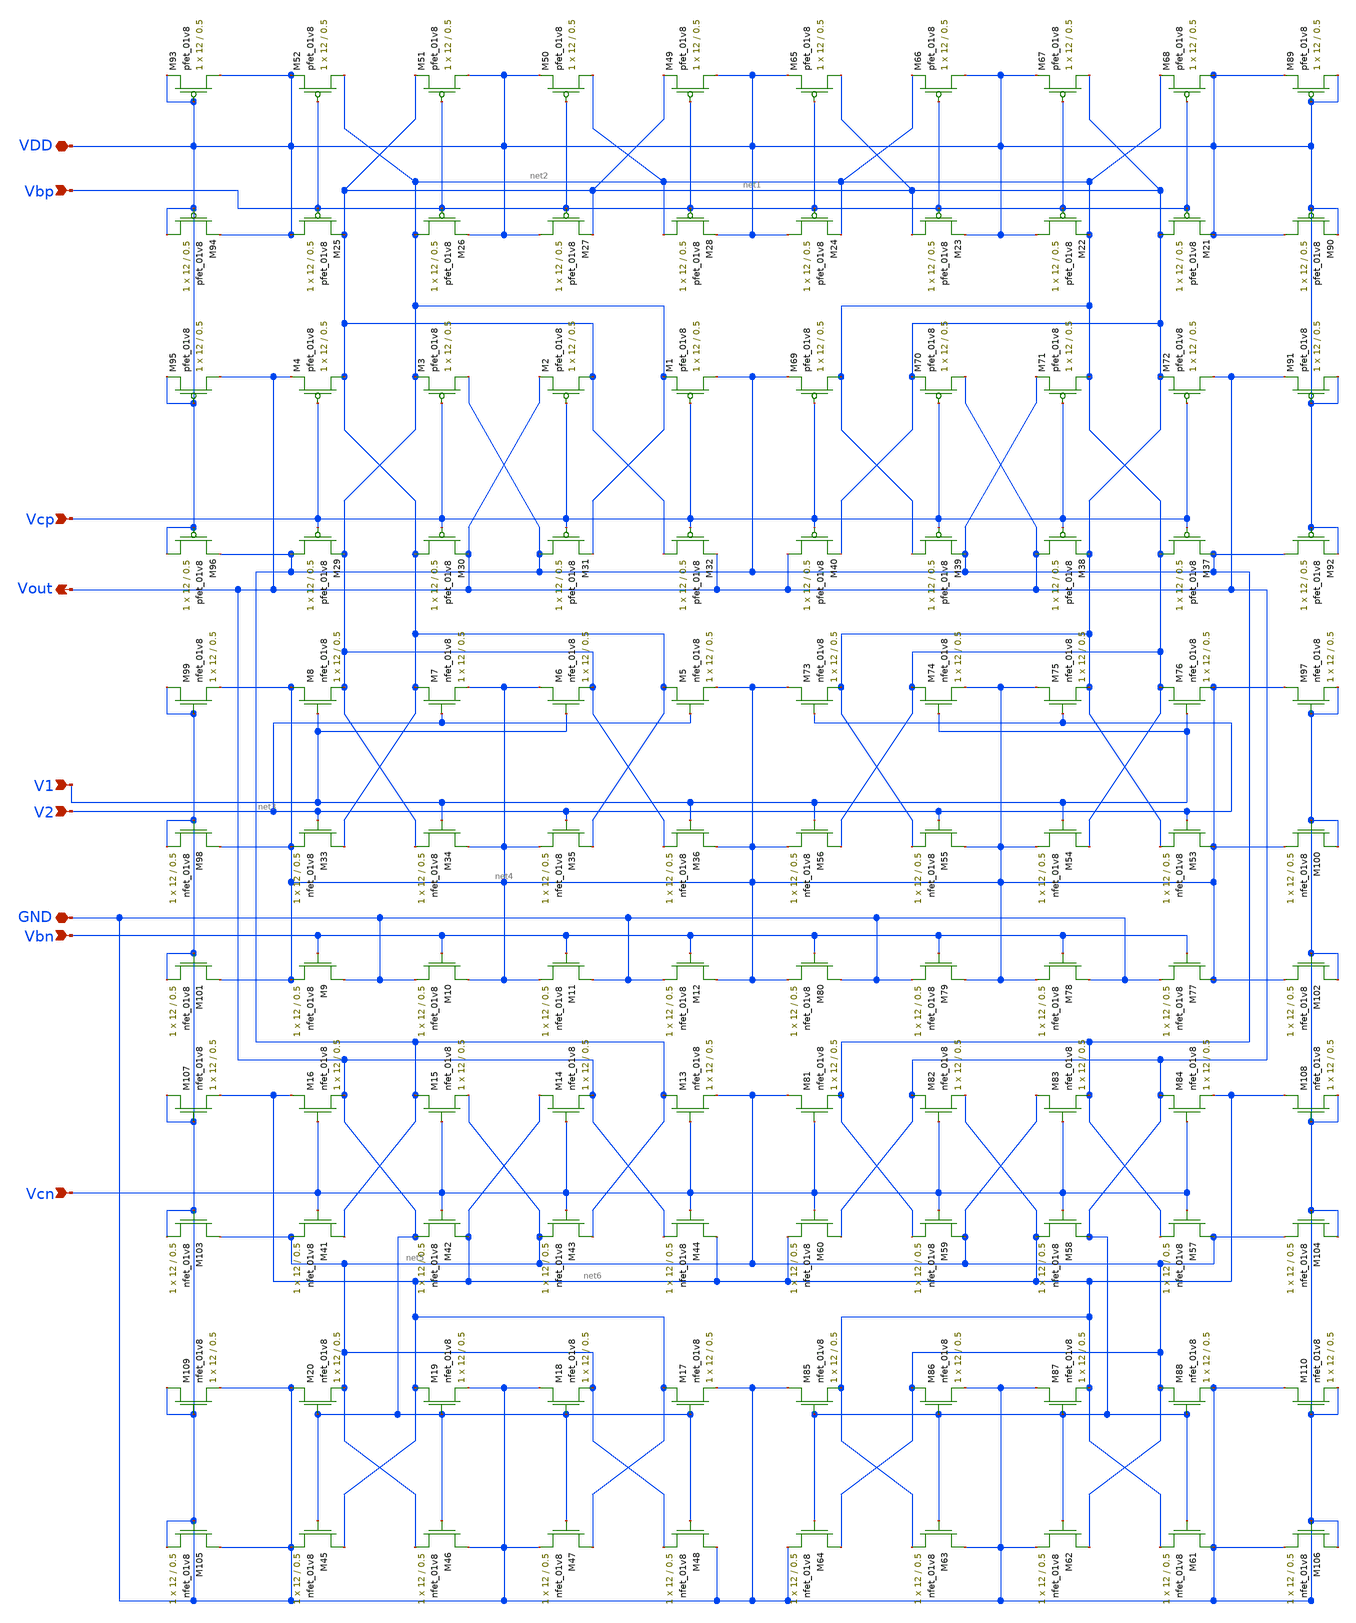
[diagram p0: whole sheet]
** sch_path: Miniproject3/layout&schematics/Folded_cascode_differential_amplifier.sch
**.subckt Folded_cascode_differential_amplifier Vbp Vcp Vout V1 V2 Vbn VDD GND Vcn
*.ipin Vbp
*.ipin Vcp
*.opin Vout
*.ipin V1
*.ipin V2
*.ipin Vbn
*.iopin VDD
*.iopin GND
*.ipin Vcn
XM52 net2 Vbp VDD VDD sky130_fd_pr__pfet_01v8 L=0.5 W=12 nf=1 ad='int((nf+1)/2) * W/nf * 0.29' as='int((nf+2)/2) * W/nf * 0.29'
+ pd='2*int((nf+1)/2) * (W/nf + 0.29)' ps='2*int((nf+2)/2) * (W/nf + 0.29)' nrd='0.29 / W' nrs='0.29 / W'
+ sa=0 sb=0 sd=0 mult=1 m=1
XM51 VDD Vbp net1 VDD sky130_fd_pr__pfet_01v8 L=0.5 W=12 nf=1 ad='int((nf+1)/2) * W/nf * 0.29' as='int((nf+2)/2) * W/nf * 0.29'
+ pd='2*int((nf+1)/2) * (W/nf + 0.29)' ps='2*int((nf+2)/2) * (W/nf + 0.29)' nrd='0.29 / W' nrs='0.29 / W'
+ sa=0 sb=0 sd=0 mult=1 m=1
XM50 net2 Vbp VDD VDD sky130_fd_pr__pfet_01v8 L=0.5 W=12 nf=1 ad='int((nf+1)/2) * W/nf * 0.29' as='int((nf+2)/2) * W/nf * 0.29'
+ pd='2*int((nf+1)/2) * (W/nf + 0.29)' ps='2*int((nf+2)/2) * (W/nf + 0.29)' nrd='0.29 / W' nrs='0.29 / W'
+ sa=0 sb=0 sd=0 mult=1 m=1
XM49 VDD Vbp net1 VDD sky130_fd_pr__pfet_01v8 L=0.5 W=12 nf=1 ad='int((nf+1)/2) * W/nf * 0.29' as='int((nf+2)/2) * W/nf * 0.29'
+ pd='2*int((nf+1)/2) * (W/nf + 0.29)' ps='2*int((nf+2)/2) * (W/nf + 0.29)' nrd='0.29 / W' nrs='0.29 / W'
+ sa=0 sb=0 sd=0 mult=1 m=1
XM65 net1 Vbp VDD VDD sky130_fd_pr__pfet_01v8 L=0.5 W=12 nf=1 ad='int((nf+1)/2) * W/nf * 0.29' as='int((nf+2)/2) * W/nf * 0.29'
+ pd='2*int((nf+1)/2) * (W/nf + 0.29)' ps='2*int((nf+2)/2) * (W/nf + 0.29)' nrd='0.29 / W' nrs='0.29 / W'
+ sa=0 sb=0 sd=0 mult=1 m=1
XM66 VDD Vbp net2 VDD sky130_fd_pr__pfet_01v8 L=0.5 W=12 nf=1 ad='int((nf+1)/2) * W/nf * 0.29' as='int((nf+2)/2) * W/nf * 0.29'
+ pd='2*int((nf+1)/2) * (W/nf + 0.29)' ps='2*int((nf+2)/2) * (W/nf + 0.29)' nrd='0.29 / W' nrs='0.29 / W'
+ sa=0 sb=0 sd=0 mult=1 m=1
XM67 net1 Vbp VDD VDD sky130_fd_pr__pfet_01v8 L=0.5 W=12 nf=1 ad='int((nf+1)/2) * W/nf * 0.29' as='int((nf+2)/2) * W/nf * 0.29'
+ pd='2*int((nf+1)/2) * (W/nf + 0.29)' ps='2*int((nf+2)/2) * (W/nf + 0.29)' nrd='0.29 / W' nrs='0.29 / W'
+ sa=0 sb=0 sd=0 mult=1 m=1
XM68 VDD Vbp net2 VDD sky130_fd_pr__pfet_01v8 L=0.5 W=12 nf=1 ad='int((nf+1)/2) * W/nf * 0.29' as='int((nf+2)/2) * W/nf * 0.29'
+ pd='2*int((nf+1)/2) * (W/nf + 0.29)' ps='2*int((nf+2)/2) * (W/nf + 0.29)' nrd='0.29 / W' nrs='0.29 / W'
+ sa=0 sb=0 sd=0 mult=1 m=1
XM89 VDD VDD VDD VDD sky130_fd_pr__pfet_01v8 L=0.5 W=12 nf=1 ad='int((nf+1)/2) * W/nf * 0.29' as='int((nf+2)/2) * W/nf * 0.29'
+ pd='2*int((nf+1)/2) * (W/nf + 0.29)' ps='2*int((nf+2)/2) * (W/nf + 0.29)' nrd='0.29 / W' nrs='0.29 / W'
+ sa=0 sb=0 sd=0 mult=1 m=1
XM93 VDD VDD VDD VDD sky130_fd_pr__pfet_01v8 L=0.5 W=12 nf=1 ad='int((nf+1)/2) * W/nf * 0.29' as='int((nf+2)/2) * W/nf * 0.29'
+ pd='2*int((nf+1)/2) * (W/nf + 0.29)' ps='2*int((nf+2)/2) * (W/nf + 0.29)' nrd='0.29 / W' nrs='0.29 / W'
+ sa=0 sb=0 sd=0 mult=1 m=1
XM94 VDD VDD VDD VDD sky130_fd_pr__pfet_01v8 L=0.5 W=12 nf=1 ad='int((nf+1)/2) * W/nf * 0.29' as='int((nf+2)/2) * W/nf * 0.29'
+ pd='2*int((nf+1)/2) * (W/nf + 0.29)' ps='2*int((nf+2)/2) * (W/nf + 0.29)' nrd='0.29 / W' nrs='0.29 / W'
+ sa=0 sb=0 sd=0 mult=1 m=1
XM25 VDD Vbp net1 VDD sky130_fd_pr__pfet_01v8 L=0.5 W=12 nf=1 ad='int((nf+1)/2) * W/nf * 0.29' as='int((nf+2)/2) * W/nf * 0.29'
+ pd='2*int((nf+1)/2) * (W/nf + 0.29)' ps='2*int((nf+2)/2) * (W/nf + 0.29)' nrd='0.29 / W' nrs='0.29 / W'
+ sa=0 sb=0 sd=0 mult=1 m=1
XM26 net2 Vbp VDD VDD sky130_fd_pr__pfet_01v8 L=0.5 W=12 nf=1 ad='int((nf+1)/2) * W/nf * 0.29' as='int((nf+2)/2) * W/nf * 0.29'
+ pd='2*int((nf+1)/2) * (W/nf + 0.29)' ps='2*int((nf+2)/2) * (W/nf + 0.29)' nrd='0.29 / W' nrs='0.29 / W'
+ sa=0 sb=0 sd=0 mult=1 m=1
XM27 VDD Vbp net1 VDD sky130_fd_pr__pfet_01v8 L=0.5 W=12 nf=1 ad='int((nf+1)/2) * W/nf * 0.29' as='int((nf+2)/2) * W/nf * 0.29'
+ pd='2*int((nf+1)/2) * (W/nf + 0.29)' ps='2*int((nf+2)/2) * (W/nf + 0.29)' nrd='0.29 / W' nrs='0.29 / W'
+ sa=0 sb=0 sd=0 mult=1 m=1
XM28 net2 Vbp VDD VDD sky130_fd_pr__pfet_01v8 L=0.5 W=12 nf=1 ad='int((nf+1)/2) * W/nf * 0.29' as='int((nf+2)/2) * W/nf * 0.29'
+ pd='2*int((nf+1)/2) * (W/nf + 0.29)' ps='2*int((nf+2)/2) * (W/nf + 0.29)' nrd='0.29 / W' nrs='0.29 / W'
+ sa=0 sb=0 sd=0 mult=1 m=1
XM24 VDD Vbp net2 VDD sky130_fd_pr__pfet_01v8 L=0.5 W=12 nf=1 ad='int((nf+1)/2) * W/nf * 0.29' as='int((nf+2)/2) * W/nf * 0.29'
+ pd='2*int((nf+1)/2) * (W/nf + 0.29)' ps='2*int((nf+2)/2) * (W/nf + 0.29)' nrd='0.29 / W' nrs='0.29 / W'
+ sa=0 sb=0 sd=0 mult=1 m=1
XM23 net1 Vbp VDD VDD sky130_fd_pr__pfet_01v8 L=0.5 W=12 nf=1 ad='int((nf+1)/2) * W/nf * 0.29' as='int((nf+2)/2) * W/nf * 0.29'
+ pd='2*int((nf+1)/2) * (W/nf + 0.29)' ps='2*int((nf+2)/2) * (W/nf + 0.29)' nrd='0.29 / W' nrs='0.29 / W'
+ sa=0 sb=0 sd=0 mult=1 m=1
XM22 VDD Vbp net2 VDD sky130_fd_pr__pfet_01v8 L=0.5 W=12 nf=1 ad='int((nf+1)/2) * W/nf * 0.29' as='int((nf+2)/2) * W/nf * 0.29'
+ pd='2*int((nf+1)/2) * (W/nf + 0.29)' ps='2*int((nf+2)/2) * (W/nf + 0.29)' nrd='0.29 / W' nrs='0.29 / W'
+ sa=0 sb=0 sd=0 mult=1 m=1
XM21 net1 Vbp VDD VDD sky130_fd_pr__pfet_01v8 L=0.5 W=12 nf=1 ad='int((nf+1)/2) * W/nf * 0.29' as='int((nf+2)/2) * W/nf * 0.29'
+ pd='2*int((nf+1)/2) * (W/nf + 0.29)' ps='2*int((nf+2)/2) * (W/nf + 0.29)' nrd='0.29 / W' nrs='0.29 / W'
+ sa=0 sb=0 sd=0 mult=1 m=1
XM90 VDD VDD VDD VDD sky130_fd_pr__pfet_01v8 L=0.5 W=12 nf=1 ad='int((nf+1)/2) * W/nf * 0.29' as='int((nf+2)/2) * W/nf * 0.29'
+ pd='2*int((nf+1)/2) * (W/nf + 0.29)' ps='2*int((nf+2)/2) * (W/nf + 0.29)' nrd='0.29 / W' nrs='0.29 / W'
+ sa=0 sb=0 sd=0 mult=1 m=1
XM95 Vout VDD VDD VDD sky130_fd_pr__pfet_01v8 L=0.5 W=12 nf=1 ad='int((nf+1)/2) * W/nf * 0.29' as='int((nf+2)/2) * W/nf * 0.29'
+ pd='2*int((nf+1)/2) * (W/nf + 0.29)' ps='2*int((nf+2)/2) * (W/nf + 0.29)' nrd='0.29 / W' nrs='0.29 / W'
+ sa=0 sb=0 sd=0 mult=1 m=1
XM4 net1 Vcp Vout VDD sky130_fd_pr__pfet_01v8 L=0.5 W=12 nf=1 ad='int((nf+1)/2) * W/nf * 0.29' as='int((nf+2)/2) * W/nf * 0.29'
+ pd='2*int((nf+1)/2) * (W/nf + 0.29)' ps='2*int((nf+2)/2) * (W/nf + 0.29)' nrd='0.29 / W' nrs='0.29 / W'
+ sa=0 sb=0 sd=0 mult=1 m=1
XM3 net3 Vcp net2 VDD sky130_fd_pr__pfet_01v8 L=0.5 W=12 nf=1 ad='int((nf+1)/2) * W/nf * 0.29' as='int((nf+2)/2) * W/nf * 0.29'
+ pd='2*int((nf+1)/2) * (W/nf + 0.29)' ps='2*int((nf+2)/2) * (W/nf + 0.29)' nrd='0.29 / W' nrs='0.29 / W'
+ sa=0 sb=0 sd=0 mult=1 m=1
XM2 net1 Vcp Vout VDD sky130_fd_pr__pfet_01v8 L=0.5 W=12 nf=1 ad='int((nf+1)/2) * W/nf * 0.29' as='int((nf+2)/2) * W/nf * 0.29'
+ pd='2*int((nf+1)/2) * (W/nf + 0.29)' ps='2*int((nf+2)/2) * (W/nf + 0.29)' nrd='0.29 / W' nrs='0.29 / W'
+ sa=0 sb=0 sd=0 mult=1 m=1
XM1 net3 Vcp net2 VDD sky130_fd_pr__pfet_01v8 L=0.5 W=12 nf=1 ad='int((nf+1)/2) * W/nf * 0.29' as='int((nf+2)/2) * W/nf * 0.29'
+ pd='2*int((nf+1)/2) * (W/nf + 0.29)' ps='2*int((nf+2)/2) * (W/nf + 0.29)' nrd='0.29 / W' nrs='0.29 / W'
+ sa=0 sb=0 sd=0 mult=1 m=1
XM69 net2 Vcp net3 VDD sky130_fd_pr__pfet_01v8 L=0.5 W=12 nf=1 ad='int((nf+1)/2) * W/nf * 0.29' as='int((nf+2)/2) * W/nf * 0.29'
+ pd='2*int((nf+1)/2) * (W/nf + 0.29)' ps='2*int((nf+2)/2) * (W/nf + 0.29)' nrd='0.29 / W' nrs='0.29 / W'
+ sa=0 sb=0 sd=0 mult=1 m=1
XM70 Vout Vcp net1 VDD sky130_fd_pr__pfet_01v8 L=0.5 W=12 nf=1 ad='int((nf+1)/2) * W/nf * 0.29' as='int((nf+2)/2) * W/nf * 0.29'
+ pd='2*int((nf+1)/2) * (W/nf + 0.29)' ps='2*int((nf+2)/2) * (W/nf + 0.29)' nrd='0.29 / W' nrs='0.29 / W'
+ sa=0 sb=0 sd=0 mult=1 m=1
XM71 net2 Vcp net3 VDD sky130_fd_pr__pfet_01v8 L=0.5 W=12 nf=1 ad='int((nf+1)/2) * W/nf * 0.29' as='int((nf+2)/2) * W/nf * 0.29'
+ pd='2*int((nf+1)/2) * (W/nf + 0.29)' ps='2*int((nf+2)/2) * (W/nf + 0.29)' nrd='0.29 / W' nrs='0.29 / W'
+ sa=0 sb=0 sd=0 mult=1 m=1
XM72 Vout Vcp net1 VDD sky130_fd_pr__pfet_01v8 L=0.5 W=12 nf=1 ad='int((nf+1)/2) * W/nf * 0.29' as='int((nf+2)/2) * W/nf * 0.29'
+ pd='2*int((nf+1)/2) * (W/nf + 0.29)' ps='2*int((nf+2)/2) * (W/nf + 0.29)' nrd='0.29 / W' nrs='0.29 / W'
+ sa=0 sb=0 sd=0 mult=1 m=1
XM91 VDD VDD Vout VDD sky130_fd_pr__pfet_01v8 L=0.5 W=12 nf=1 ad='int((nf+1)/2) * W/nf * 0.29' as='int((nf+2)/2) * W/nf * 0.29'
+ pd='2*int((nf+1)/2) * (W/nf + 0.29)' ps='2*int((nf+2)/2) * (W/nf + 0.29)' nrd='0.29 / W' nrs='0.29 / W'
+ sa=0 sb=0 sd=0 mult=1 m=1
XM96 VDD VDD net3 VDD sky130_fd_pr__pfet_01v8 L=0.5 W=12 nf=1 ad='int((nf+1)/2) * W/nf * 0.29' as='int((nf+2)/2) * W/nf * 0.29'
+ pd='2*int((nf+1)/2) * (W/nf + 0.29)' ps='2*int((nf+2)/2) * (W/nf + 0.29)' nrd='0.29 / W' nrs='0.29 / W'
+ sa=0 sb=0 sd=0 mult=1 m=1
XM29 net3 Vcp net2 VDD sky130_fd_pr__pfet_01v8 L=0.5 W=12 nf=1 ad='int((nf+1)/2) * W/nf * 0.29' as='int((nf+2)/2) * W/nf * 0.29'
+ pd='2*int((nf+1)/2) * (W/nf + 0.29)' ps='2*int((nf+2)/2) * (W/nf + 0.29)' nrd='0.29 / W' nrs='0.29 / W'
+ sa=0 sb=0 sd=0 mult=1 m=1
XM30 net1 Vcp Vout VDD sky130_fd_pr__pfet_01v8 L=0.5 W=12 nf=1 ad='int((nf+1)/2) * W/nf * 0.29' as='int((nf+2)/2) * W/nf * 0.29'
+ pd='2*int((nf+1)/2) * (W/nf + 0.29)' ps='2*int((nf+2)/2) * (W/nf + 0.29)' nrd='0.29 / W' nrs='0.29 / W'
+ sa=0 sb=0 sd=0 mult=1 m=1
XM31 net3 Vcp net2 VDD sky130_fd_pr__pfet_01v8 L=0.5 W=12 nf=1 ad='int((nf+1)/2) * W/nf * 0.29' as='int((nf+2)/2) * W/nf * 0.29'
+ pd='2*int((nf+1)/2) * (W/nf + 0.29)' ps='2*int((nf+2)/2) * (W/nf + 0.29)' nrd='0.29 / W' nrs='0.29 / W'
+ sa=0 sb=0 sd=0 mult=1 m=1
XM32 net1 Vcp Vout VDD sky130_fd_pr__pfet_01v8 L=0.5 W=12 nf=1 ad='int((nf+1)/2) * W/nf * 0.29' as='int((nf+2)/2) * W/nf * 0.29'
+ pd='2*int((nf+1)/2) * (W/nf + 0.29)' ps='2*int((nf+2)/2) * (W/nf + 0.29)' nrd='0.29 / W' nrs='0.29 / W'
+ sa=0 sb=0 sd=0 mult=1 m=1
XM40 Vout Vcp net1 VDD sky130_fd_pr__pfet_01v8 L=0.5 W=12 nf=1 ad='int((nf+1)/2) * W/nf * 0.29' as='int((nf+2)/2) * W/nf * 0.29'
+ pd='2*int((nf+1)/2) * (W/nf + 0.29)' ps='2*int((nf+2)/2) * (W/nf + 0.29)' nrd='0.29 / W' nrs='0.29 / W'
+ sa=0 sb=0 sd=0 mult=1 m=1
XM39 net2 Vcp net3 VDD sky130_fd_pr__pfet_01v8 L=0.5 W=12 nf=1 ad='int((nf+1)/2) * W/nf * 0.29' as='int((nf+2)/2) * W/nf * 0.29'
+ pd='2*int((nf+1)/2) * (W/nf + 0.29)' ps='2*int((nf+2)/2) * (W/nf + 0.29)' nrd='0.29 / W' nrs='0.29 / W'
+ sa=0 sb=0 sd=0 mult=1 m=1
XM38 Vout Vcp net1 VDD sky130_fd_pr__pfet_01v8 L=0.5 W=12 nf=1 ad='int((nf+1)/2) * W/nf * 0.29' as='int((nf+2)/2) * W/nf * 0.29'
+ pd='2*int((nf+1)/2) * (W/nf + 0.29)' ps='2*int((nf+2)/2) * (W/nf + 0.29)' nrd='0.29 / W' nrs='0.29 / W'
+ sa=0 sb=0 sd=0 mult=1 m=1
XM37 net2 Vcp net3 VDD sky130_fd_pr__pfet_01v8 L=0.5 W=12 nf=1 ad='int((nf+1)/2) * W/nf * 0.29' as='int((nf+2)/2) * W/nf * 0.29'
+ pd='2*int((nf+1)/2) * (W/nf + 0.29)' ps='2*int((nf+2)/2) * (W/nf + 0.29)' nrd='0.29 / W' nrs='0.29 / W'
+ sa=0 sb=0 sd=0 mult=1 m=1
XM92 net3 VDD VDD VDD sky130_fd_pr__pfet_01v8 L=0.5 W=12 nf=1 ad='int((nf+1)/2) * W/nf * 0.29' as='int((nf+2)/2) * W/nf * 0.29'
+ pd='2*int((nf+1)/2) * (W/nf + 0.29)' ps='2*int((nf+2)/2) * (W/nf + 0.29)' nrd='0.29 / W' nrs='0.29 / W'
+ sa=0 sb=0 sd=0 mult=1 m=1
XM8 net4 V1 net2 GND sky130_fd_pr__nfet_01v8 L=0.5 W=12 nf=1 ad='int((nf+1)/2) * W/nf * 0.29' as='int((nf+2)/2) * W/nf * 0.29'
+ pd='2*int((nf+1)/2) * (W/nf + 0.29)' ps='2*int((nf+2)/2) * (W/nf + 0.29)' nrd='0.29 / W' nrs='0.29 / W'
+ sa=0 sb=0 sd=0 mult=1 m=1
XM7 net1 V2 net4 GND sky130_fd_pr__nfet_01v8 L=0.5 W=12 nf=1 ad='int((nf+1)/2) * W/nf * 0.29' as='int((nf+2)/2) * W/nf * 0.29'
+ pd='2*int((nf+1)/2) * (W/nf + 0.29)' ps='2*int((nf+2)/2) * (W/nf + 0.29)' nrd='0.29 / W' nrs='0.29 / W'
+ sa=0 sb=0 sd=0 mult=1 m=1
XM6 net4 V1 net2 GND sky130_fd_pr__nfet_01v8 L=0.5 W=12 nf=1 ad='int((nf+1)/2) * W/nf * 0.29' as='int((nf+2)/2) * W/nf * 0.29'
+ pd='2*int((nf+1)/2) * (W/nf + 0.29)' ps='2*int((nf+2)/2) * (W/nf + 0.29)' nrd='0.29 / W' nrs='0.29 / W'
+ sa=0 sb=0 sd=0 mult=1 m=1
XM5 net1 V2 net4 GND sky130_fd_pr__nfet_01v8 L=0.5 W=12 nf=1 ad='int((nf+1)/2) * W/nf * 0.29' as='int((nf+2)/2) * W/nf * 0.29'
+ pd='2*int((nf+1)/2) * (W/nf + 0.29)' ps='2*int((nf+2)/2) * (W/nf + 0.29)' nrd='0.29 / W' nrs='0.29 / W'
+ sa=0 sb=0 sd=0 mult=1 m=1
XM73 net4 V2 net1 GND sky130_fd_pr__nfet_01v8 L=0.5 W=12 nf=1 ad='int((nf+1)/2) * W/nf * 0.29' as='int((nf+2)/2) * W/nf * 0.29'
+ pd='2*int((nf+1)/2) * (W/nf + 0.29)' ps='2*int((nf+2)/2) * (W/nf + 0.29)' nrd='0.29 / W' nrs='0.29 / W'
+ sa=0 sb=0 sd=0 mult=1 m=1
XM74 net2 V1 net4 GND sky130_fd_pr__nfet_01v8 L=0.5 W=12 nf=1 ad='int((nf+1)/2) * W/nf * 0.29' as='int((nf+2)/2) * W/nf * 0.29'
+ pd='2*int((nf+1)/2) * (W/nf + 0.29)' ps='2*int((nf+2)/2) * (W/nf + 0.29)' nrd='0.29 / W' nrs='0.29 / W'
+ sa=0 sb=0 sd=0 mult=1 m=1
XM75 net4 V2 net1 GND sky130_fd_pr__nfet_01v8 L=0.5 W=12 nf=1 ad='int((nf+1)/2) * W/nf * 0.29' as='int((nf+2)/2) * W/nf * 0.29'
+ pd='2*int((nf+1)/2) * (W/nf + 0.29)' ps='2*int((nf+2)/2) * (W/nf + 0.29)' nrd='0.29 / W' nrs='0.29 / W'
+ sa=0 sb=0 sd=0 mult=1 m=1
XM76 net2 V1 net4 GND sky130_fd_pr__nfet_01v8 L=0.5 W=12 nf=1 ad='int((nf+1)/2) * W/nf * 0.29' as='int((nf+2)/2) * W/nf * 0.29'
+ pd='2*int((nf+1)/2) * (W/nf + 0.29)' ps='2*int((nf+2)/2) * (W/nf + 0.29)' nrd='0.29 / W' nrs='0.29 / W'
+ sa=0 sb=0 sd=0 mult=1 m=1
XM97 net4 GND GND GND sky130_fd_pr__nfet_01v8 L=0.5 W=12 nf=1 ad='int((nf+1)/2) * W/nf * 0.29' as='int((nf+2)/2) * W/nf * 0.29'
+ pd='2*int((nf+1)/2) * (W/nf + 0.29)' ps='2*int((nf+2)/2) * (W/nf + 0.29)' nrd='0.29 / W' nrs='0.29 / W'
+ sa=0 sb=0 sd=0 mult=1 m=1
XM98 net4 GND GND GND sky130_fd_pr__nfet_01v8 L=0.5 W=12 nf=1 ad='int((nf+1)/2) * W/nf * 0.29' as='int((nf+2)/2) * W/nf * 0.29'
+ pd='2*int((nf+1)/2) * (W/nf + 0.29)' ps='2*int((nf+2)/2) * (W/nf + 0.29)' nrd='0.29 / W' nrs='0.29 / W'
+ sa=0 sb=0 sd=0 mult=1 m=1
XM99 GND GND net4 GND sky130_fd_pr__nfet_01v8 L=0.5 W=12 nf=1 ad='int((nf+1)/2) * W/nf * 0.29' as='int((nf+2)/2) * W/nf * 0.29'
+ pd='2*int((nf+1)/2) * (W/nf + 0.29)' ps='2*int((nf+2)/2) * (W/nf + 0.29)' nrd='0.29 / W' nrs='0.29 / W'
+ sa=0 sb=0 sd=0 mult=1 m=1
XM33 net1 V2 net4 GND sky130_fd_pr__nfet_01v8 L=0.5 W=12 nf=1 ad='int((nf+1)/2) * W/nf * 0.29' as='int((nf+2)/2) * W/nf * 0.29'
+ pd='2*int((nf+1)/2) * (W/nf + 0.29)' ps='2*int((nf+2)/2) * (W/nf + 0.29)' nrd='0.29 / W' nrs='0.29 / W'
+ sa=0 sb=0 sd=0 mult=1 m=1
XM34 net4 V1 net2 GND sky130_fd_pr__nfet_01v8 L=0.5 W=12 nf=1 ad='int((nf+1)/2) * W/nf * 0.29' as='int((nf+2)/2) * W/nf * 0.29'
+ pd='2*int((nf+1)/2) * (W/nf + 0.29)' ps='2*int((nf+2)/2) * (W/nf + 0.29)' nrd='0.29 / W' nrs='0.29 / W'
+ sa=0 sb=0 sd=0 mult=1 m=1
XM35 net1 V2 net4 GND sky130_fd_pr__nfet_01v8 L=0.5 W=12 nf=1 ad='int((nf+1)/2) * W/nf * 0.29' as='int((nf+2)/2) * W/nf * 0.29'
+ pd='2*int((nf+1)/2) * (W/nf + 0.29)' ps='2*int((nf+2)/2) * (W/nf + 0.29)' nrd='0.29 / W' nrs='0.29 / W'
+ sa=0 sb=0 sd=0 mult=1 m=1
XM36 net4 V1 net2 GND sky130_fd_pr__nfet_01v8 L=0.5 W=12 nf=1 ad='int((nf+1)/2) * W/nf * 0.29' as='int((nf+2)/2) * W/nf * 0.29'
+ pd='2*int((nf+1)/2) * (W/nf + 0.29)' ps='2*int((nf+2)/2) * (W/nf + 0.29)' nrd='0.29 / W' nrs='0.29 / W'
+ sa=0 sb=0 sd=0 mult=1 m=1
XM56 net2 V1 net4 GND sky130_fd_pr__nfet_01v8 L=0.5 W=12 nf=1 ad='int((nf+1)/2) * W/nf * 0.29' as='int((nf+2)/2) * W/nf * 0.29'
+ pd='2*int((nf+1)/2) * (W/nf + 0.29)' ps='2*int((nf+2)/2) * (W/nf + 0.29)' nrd='0.29 / W' nrs='0.29 / W'
+ sa=0 sb=0 sd=0 mult=1 m=1
XM55 net4 V2 net1 GND sky130_fd_pr__nfet_01v8 L=0.5 W=12 nf=1 ad='int((nf+1)/2) * W/nf * 0.29' as='int((nf+2)/2) * W/nf * 0.29'
+ pd='2*int((nf+1)/2) * (W/nf + 0.29)' ps='2*int((nf+2)/2) * (W/nf + 0.29)' nrd='0.29 / W' nrs='0.29 / W'
+ sa=0 sb=0 sd=0 mult=1 m=1
XM54 net2 V1 net4 GND sky130_fd_pr__nfet_01v8 L=0.5 W=12 nf=1 ad='int((nf+1)/2) * W/nf * 0.29' as='int((nf+2)/2) * W/nf * 0.29'
+ pd='2*int((nf+1)/2) * (W/nf + 0.29)' ps='2*int((nf+2)/2) * (W/nf + 0.29)' nrd='0.29 / W' nrs='0.29 / W'
+ sa=0 sb=0 sd=0 mult=1 m=1
XM53 net4 V2 net1 GND sky130_fd_pr__nfet_01v8 L=0.5 W=12 nf=1 ad='int((nf+1)/2) * W/nf * 0.29' as='int((nf+2)/2) * W/nf * 0.29'
+ pd='2*int((nf+1)/2) * (W/nf + 0.29)' ps='2*int((nf+2)/2) * (W/nf + 0.29)' nrd='0.29 / W' nrs='0.29 / W'
+ sa=0 sb=0 sd=0 mult=1 m=1
XM100 GND GND net4 GND sky130_fd_pr__nfet_01v8 L=0.5 W=12 nf=1 ad='int((nf+1)/2) * W/nf * 0.29' as='int((nf+2)/2) * W/nf * 0.29'
+ pd='2*int((nf+1)/2) * (W/nf + 0.29)' ps='2*int((nf+2)/2) * (W/nf + 0.29)' nrd='0.29 / W' nrs='0.29 / W'
+ sa=0 sb=0 sd=0 mult=1 m=1
XM101 net4 GND GND GND sky130_fd_pr__nfet_01v8 L=0.5 W=12 nf=1 ad='int((nf+1)/2) * W/nf * 0.29' as='int((nf+2)/2) * W/nf * 0.29'
+ pd='2*int((nf+1)/2) * (W/nf + 0.29)' ps='2*int((nf+2)/2) * (W/nf + 0.29)' nrd='0.29 / W' nrs='0.29 / W'
+ sa=0 sb=0 sd=0 mult=1 m=1
XM9 GND Vbn net4 GND sky130_fd_pr__nfet_01v8 L=0.5 W=12 nf=1 ad='int((nf+1)/2) * W/nf * 0.29' as='int((nf+2)/2) * W/nf * 0.29'
+ pd='2*int((nf+1)/2) * (W/nf + 0.29)' ps='2*int((nf+2)/2) * (W/nf + 0.29)' nrd='0.29 / W' nrs='0.29 / W'
+ sa=0 sb=0 sd=0 mult=1 m=1
XM10 net4 Vbn GND GND sky130_fd_pr__nfet_01v8 L=0.5 W=12 nf=1 ad='int((nf+1)/2) * W/nf * 0.29' as='int((nf+2)/2) * W/nf * 0.29'
+ pd='2*int((nf+1)/2) * (W/nf + 0.29)' ps='2*int((nf+2)/2) * (W/nf + 0.29)' nrd='0.29 / W' nrs='0.29 / W'
+ sa=0 sb=0 sd=0 mult=1 m=1
XM11 GND Vbn net4 GND sky130_fd_pr__nfet_01v8 L=0.5 W=12 nf=1 ad='int((nf+1)/2) * W/nf * 0.29' as='int((nf+2)/2) * W/nf * 0.29'
+ pd='2*int((nf+1)/2) * (W/nf + 0.29)' ps='2*int((nf+2)/2) * (W/nf + 0.29)' nrd='0.29 / W' nrs='0.29 / W'
+ sa=0 sb=0 sd=0 mult=1 m=1
XM12 net4 Vbn GND GND sky130_fd_pr__nfet_01v8 L=0.5 W=12 nf=1 ad='int((nf+1)/2) * W/nf * 0.29' as='int((nf+2)/2) * W/nf * 0.29'
+ pd='2*int((nf+1)/2) * (W/nf + 0.29)' ps='2*int((nf+2)/2) * (W/nf + 0.29)' nrd='0.29 / W' nrs='0.29 / W'
+ sa=0 sb=0 sd=0 mult=1 m=1
XM80 GND Vbn net4 GND sky130_fd_pr__nfet_01v8 L=0.5 W=12 nf=1 ad='int((nf+1)/2) * W/nf * 0.29' as='int((nf+2)/2) * W/nf * 0.29'
+ pd='2*int((nf+1)/2) * (W/nf + 0.29)' ps='2*int((nf+2)/2) * (W/nf + 0.29)' nrd='0.29 / W' nrs='0.29 / W'
+ sa=0 sb=0 sd=0 mult=1 m=1
XM79 net4 Vbn GND GND sky130_fd_pr__nfet_01v8 L=0.5 W=12 nf=1 ad='int((nf+1)/2) * W/nf * 0.29' as='int((nf+2)/2) * W/nf * 0.29'
+ pd='2*int((nf+1)/2) * (W/nf + 0.29)' ps='2*int((nf+2)/2) * (W/nf + 0.29)' nrd='0.29 / W' nrs='0.29 / W'
+ sa=0 sb=0 sd=0 mult=1 m=1
XM78 GND Vbn net4 GND sky130_fd_pr__nfet_01v8 L=0.5 W=12 nf=1 ad='int((nf+1)/2) * W/nf * 0.29' as='int((nf+2)/2) * W/nf * 0.29'
+ pd='2*int((nf+1)/2) * (W/nf + 0.29)' ps='2*int((nf+2)/2) * (W/nf + 0.29)' nrd='0.29 / W' nrs='0.29 / W'
+ sa=0 sb=0 sd=0 mult=1 m=1
XM77 net4 Vbn GND GND sky130_fd_pr__nfet_01v8 L=0.5 W=12 nf=1 ad='int((nf+1)/2) * W/nf * 0.29' as='int((nf+2)/2) * W/nf * 0.29'
+ pd='2*int((nf+1)/2) * (W/nf + 0.29)' ps='2*int((nf+2)/2) * (W/nf + 0.29)' nrd='0.29 / W' nrs='0.29 / W'
+ sa=0 sb=0 sd=0 mult=1 m=1
XM102 GND GND net4 GND sky130_fd_pr__nfet_01v8 L=0.5 W=12 nf=1 ad='int((nf+1)/2) * W/nf * 0.29' as='int((nf+2)/2) * W/nf * 0.29'
+ pd='2*int((nf+1)/2) * (W/nf + 0.29)' ps='2*int((nf+2)/2) * (W/nf + 0.29)' nrd='0.29 / W' nrs='0.29 / W'
+ sa=0 sb=0 sd=0 mult=1 m=1
XM103 net5 GND GND GND sky130_fd_pr__nfet_01v8 L=0.5 W=12 nf=1 ad='int((nf+1)/2) * W/nf * 0.29' as='int((nf+2)/2) * W/nf * 0.29'
+ pd='2*int((nf+1)/2) * (W/nf + 0.29)' ps='2*int((nf+2)/2) * (W/nf + 0.29)' nrd='0.29 / W' nrs='0.29 / W'
+ sa=0 sb=0 sd=0 mult=1 m=1
XM41 net3 Vcn net5 GND sky130_fd_pr__nfet_01v8 L=0.5 W=12 nf=1 ad='int((nf+1)/2) * W/nf * 0.29' as='int((nf+2)/2) * W/nf * 0.29'
+ pd='2*int((nf+1)/2) * (W/nf + 0.29)' ps='2*int((nf+2)/2) * (W/nf + 0.29)' nrd='0.29 / W' nrs='0.29 / W'
+ sa=0 sb=0 sd=0 mult=1 m=1
XM42 net6 Vcn Vout GND sky130_fd_pr__nfet_01v8 L=0.5 W=12 nf=1 ad='int((nf+1)/2) * W/nf * 0.29' as='int((nf+2)/2) * W/nf * 0.29'
+ pd='2*int((nf+1)/2) * (W/nf + 0.29)' ps='2*int((nf+2)/2) * (W/nf + 0.29)' nrd='0.29 / W' nrs='0.29 / W'
+ sa=0 sb=0 sd=0 mult=1 m=1
XM43 net3 Vcn net5 GND sky130_fd_pr__nfet_01v8 L=0.5 W=12 nf=1 ad='int((nf+1)/2) * W/nf * 0.29' as='int((nf+2)/2) * W/nf * 0.29'
+ pd='2*int((nf+1)/2) * (W/nf + 0.29)' ps='2*int((nf+2)/2) * (W/nf + 0.29)' nrd='0.29 / W' nrs='0.29 / W'
+ sa=0 sb=0 sd=0 mult=1 m=1
XM44 net6 Vcn Vout GND sky130_fd_pr__nfet_01v8 L=0.5 W=12 nf=1 ad='int((nf+1)/2) * W/nf * 0.29' as='int((nf+2)/2) * W/nf * 0.29'
+ pd='2*int((nf+1)/2) * (W/nf + 0.29)' ps='2*int((nf+2)/2) * (W/nf + 0.29)' nrd='0.29 / W' nrs='0.29 / W'
+ sa=0 sb=0 sd=0 mult=1 m=1
XM60 Vout Vcn net6 GND sky130_fd_pr__nfet_01v8 L=0.5 W=12 nf=1 ad='int((nf+1)/2) * W/nf * 0.29' as='int((nf+2)/2) * W/nf * 0.29'
+ pd='2*int((nf+1)/2) * (W/nf + 0.29)' ps='2*int((nf+2)/2) * (W/nf + 0.29)' nrd='0.29 / W' nrs='0.29 / W'
+ sa=0 sb=0 sd=0 mult=1 m=1
XM59 net5 Vcn net3 GND sky130_fd_pr__nfet_01v8 L=0.5 W=12 nf=1 ad='int((nf+1)/2) * W/nf * 0.29' as='int((nf+2)/2) * W/nf * 0.29'
+ pd='2*int((nf+1)/2) * (W/nf + 0.29)' ps='2*int((nf+2)/2) * (W/nf + 0.29)' nrd='0.29 / W' nrs='0.29 / W'
+ sa=0 sb=0 sd=0 mult=1 m=1
XM58 Vout Vcn net6 GND sky130_fd_pr__nfet_01v8 L=0.5 W=12 nf=1 ad='int((nf+1)/2) * W/nf * 0.29' as='int((nf+2)/2) * W/nf * 0.29'
+ pd='2*int((nf+1)/2) * (W/nf + 0.29)' ps='2*int((nf+2)/2) * (W/nf + 0.29)' nrd='0.29 / W' nrs='0.29 / W'
+ sa=0 sb=0 sd=0 mult=1 m=1
XM57 net5 Vcn net3 GND sky130_fd_pr__nfet_01v8 L=0.5 W=12 nf=1 ad='int((nf+1)/2) * W/nf * 0.29' as='int((nf+2)/2) * W/nf * 0.29'
+ pd='2*int((nf+1)/2) * (W/nf + 0.29)' ps='2*int((nf+2)/2) * (W/nf + 0.29)' nrd='0.29 / W' nrs='0.29 / W'
+ sa=0 sb=0 sd=0 mult=1 m=1
XM104 GND GND net5 GND sky130_fd_pr__nfet_01v8 L=0.5 W=12 nf=1 ad='int((nf+1)/2) * W/nf * 0.29' as='int((nf+2)/2) * W/nf * 0.29'
+ pd='2*int((nf+1)/2) * (W/nf + 0.29)' ps='2*int((nf+2)/2) * (W/nf + 0.29)' nrd='0.29 / W' nrs='0.29 / W'
+ sa=0 sb=0 sd=0 mult=1 m=1
XM105 GND GND GND GND sky130_fd_pr__nfet_01v8 L=0.5 W=12 nf=1 ad='int((nf+1)/2) * W/nf * 0.29' as='int((nf+2)/2) * W/nf * 0.29'
+ pd='2*int((nf+1)/2) * (W/nf + 0.29)' ps='2*int((nf+2)/2) * (W/nf + 0.29)' nrd='0.29 / W' nrs='0.29 / W'
+ sa=0 sb=0 sd=0 mult=1 m=1
XM45 net6 Vout GND GND sky130_fd_pr__nfet_01v8 L=0.5 W=12 nf=1 ad='int((nf+1)/2) * W/nf * 0.29' as='int((nf+2)/2) * W/nf * 0.29'
+ pd='2*int((nf+1)/2) * (W/nf + 0.29)' ps='2*int((nf+2)/2) * (W/nf + 0.29)' nrd='0.29 / W' nrs='0.29 / W'
+ sa=0 sb=0 sd=0 mult=1 m=1
XM46 GND Vout net5 GND sky130_fd_pr__nfet_01v8 L=0.5 W=12 nf=1 ad='int((nf+1)/2) * W/nf * 0.29' as='int((nf+2)/2) * W/nf * 0.29'
+ pd='2*int((nf+1)/2) * (W/nf + 0.29)' ps='2*int((nf+2)/2) * (W/nf + 0.29)' nrd='0.29 / W' nrs='0.29 / W'
+ sa=0 sb=0 sd=0 mult=1 m=1
XM47 net6 Vout GND GND sky130_fd_pr__nfet_01v8 L=0.5 W=12 nf=1 ad='int((nf+1)/2) * W/nf * 0.29' as='int((nf+2)/2) * W/nf * 0.29'
+ pd='2*int((nf+1)/2) * (W/nf + 0.29)' ps='2*int((nf+2)/2) * (W/nf + 0.29)' nrd='0.29 / W' nrs='0.29 / W'
+ sa=0 sb=0 sd=0 mult=1 m=1
XM48 GND Vout net5 GND sky130_fd_pr__nfet_01v8 L=0.5 W=12 nf=1 ad='int((nf+1)/2) * W/nf * 0.29' as='int((nf+2)/2) * W/nf * 0.29'
+ pd='2*int((nf+1)/2) * (W/nf + 0.29)' ps='2*int((nf+2)/2) * (W/nf + 0.29)' nrd='0.29 / W' nrs='0.29 / W'
+ sa=0 sb=0 sd=0 mult=1 m=1
XM64 net5 Vout GND GND sky130_fd_pr__nfet_01v8 L=0.5 W=12 nf=1 ad='int((nf+1)/2) * W/nf * 0.29' as='int((nf+2)/2) * W/nf * 0.29'
+ pd='2*int((nf+1)/2) * (W/nf + 0.29)' ps='2*int((nf+2)/2) * (W/nf + 0.29)' nrd='0.29 / W' nrs='0.29 / W'
+ sa=0 sb=0 sd=0 mult=1 m=1
XM63 GND Vout net6 GND sky130_fd_pr__nfet_01v8 L=0.5 W=12 nf=1 ad='int((nf+1)/2) * W/nf * 0.29' as='int((nf+2)/2) * W/nf * 0.29'
+ pd='2*int((nf+1)/2) * (W/nf + 0.29)' ps='2*int((nf+2)/2) * (W/nf + 0.29)' nrd='0.29 / W' nrs='0.29 / W'
+ sa=0 sb=0 sd=0 mult=1 m=1
XM62 net5 Vout GND GND sky130_fd_pr__nfet_01v8 L=0.5 W=12 nf=1 ad='int((nf+1)/2) * W/nf * 0.29' as='int((nf+2)/2) * W/nf * 0.29'
+ pd='2*int((nf+1)/2) * (W/nf + 0.29)' ps='2*int((nf+2)/2) * (W/nf + 0.29)' nrd='0.29 / W' nrs='0.29 / W'
+ sa=0 sb=0 sd=0 mult=1 m=1
XM61 GND Vout net6 GND sky130_fd_pr__nfet_01v8 L=0.5 W=12 nf=1 ad='int((nf+1)/2) * W/nf * 0.29' as='int((nf+2)/2) * W/nf * 0.29'
+ pd='2*int((nf+1)/2) * (W/nf + 0.29)' ps='2*int((nf+2)/2) * (W/nf + 0.29)' nrd='0.29 / W' nrs='0.29 / W'
+ sa=0 sb=0 sd=0 mult=1 m=1
XM106 GND GND GND GND sky130_fd_pr__nfet_01v8 L=0.5 W=12 nf=1 ad='int((nf+1)/2) * W/nf * 0.29' as='int((nf+2)/2) * W/nf * 0.29'
+ pd='2*int((nf+1)/2) * (W/nf + 0.29)' ps='2*int((nf+2)/2) * (W/nf + 0.29)' nrd='0.29 / W' nrs='0.29 / W'
+ sa=0 sb=0 sd=0 mult=1 m=1
XM107 GND GND net6 GND sky130_fd_pr__nfet_01v8 L=0.5 W=12 nf=1 ad='int((nf+1)/2) * W/nf * 0.29' as='int((nf+2)/2) * W/nf * 0.29'
+ pd='2*int((nf+1)/2) * (W/nf + 0.29)' ps='2*int((nf+2)/2) * (W/nf + 0.29)' nrd='0.29 / W' nrs='0.29 / W'
+ sa=0 sb=0 sd=0 mult=1 m=1
XM16 net6 Vcn Vout GND sky130_fd_pr__nfet_01v8 L=0.5 W=12 nf=1 ad='int((nf+1)/2) * W/nf * 0.29' as='int((nf+2)/2) * W/nf * 0.29'
+ pd='2*int((nf+1)/2) * (W/nf + 0.29)' ps='2*int((nf+2)/2) * (W/nf + 0.29)' nrd='0.29 / W' nrs='0.29 / W'
+ sa=0 sb=0 sd=0 mult=1 m=1
XM15 net3 Vcn net5 GND sky130_fd_pr__nfet_01v8 L=0.5 W=12 nf=1 ad='int((nf+1)/2) * W/nf * 0.29' as='int((nf+2)/2) * W/nf * 0.29'
+ pd='2*int((nf+1)/2) * (W/nf + 0.29)' ps='2*int((nf+2)/2) * (W/nf + 0.29)' nrd='0.29 / W' nrs='0.29 / W'
+ sa=0 sb=0 sd=0 mult=1 m=1
XM14 net6 Vcn Vout GND sky130_fd_pr__nfet_01v8 L=0.5 W=12 nf=1 ad='int((nf+1)/2) * W/nf * 0.29' as='int((nf+2)/2) * W/nf * 0.29'
+ pd='2*int((nf+1)/2) * (W/nf + 0.29)' ps='2*int((nf+2)/2) * (W/nf + 0.29)' nrd='0.29 / W' nrs='0.29 / W'
+ sa=0 sb=0 sd=0 mult=1 m=1
XM13 net3 Vcn net5 GND sky130_fd_pr__nfet_01v8 L=0.5 W=12 nf=1 ad='int((nf+1)/2) * W/nf * 0.29' as='int((nf+2)/2) * W/nf * 0.29'
+ pd='2*int((nf+1)/2) * (W/nf + 0.29)' ps='2*int((nf+2)/2) * (W/nf + 0.29)' nrd='0.29 / W' nrs='0.29 / W'
+ sa=0 sb=0 sd=0 mult=1 m=1
XM81 net5 Vcn net3 GND sky130_fd_pr__nfet_01v8 L=0.5 W=12 nf=1 ad='int((nf+1)/2) * W/nf * 0.29' as='int((nf+2)/2) * W/nf * 0.29'
+ pd='2*int((nf+1)/2) * (W/nf + 0.29)' ps='2*int((nf+2)/2) * (W/nf + 0.29)' nrd='0.29 / W' nrs='0.29 / W'
+ sa=0 sb=0 sd=0 mult=1 m=1
XM82 Vout Vcn net6 GND sky130_fd_pr__nfet_01v8 L=0.5 W=12 nf=1 ad='int((nf+1)/2) * W/nf * 0.29' as='int((nf+2)/2) * W/nf * 0.29'
+ pd='2*int((nf+1)/2) * (W/nf + 0.29)' ps='2*int((nf+2)/2) * (W/nf + 0.29)' nrd='0.29 / W' nrs='0.29 / W'
+ sa=0 sb=0 sd=0 mult=1 m=1
XM83 net5 Vcn net3 GND sky130_fd_pr__nfet_01v8 L=0.5 W=12 nf=1 ad='int((nf+1)/2) * W/nf * 0.29' as='int((nf+2)/2) * W/nf * 0.29'
+ pd='2*int((nf+1)/2) * (W/nf + 0.29)' ps='2*int((nf+2)/2) * (W/nf + 0.29)' nrd='0.29 / W' nrs='0.29 / W'
+ sa=0 sb=0 sd=0 mult=1 m=1
XM84 Vout Vcn net6 GND sky130_fd_pr__nfet_01v8 L=0.5 W=12 nf=1 ad='int((nf+1)/2) * W/nf * 0.29' as='int((nf+2)/2) * W/nf * 0.29'
+ pd='2*int((nf+1)/2) * (W/nf + 0.29)' ps='2*int((nf+2)/2) * (W/nf + 0.29)' nrd='0.29 / W' nrs='0.29 / W'
+ sa=0 sb=0 sd=0 mult=1 m=1
XM108 net6 GND GND GND sky130_fd_pr__nfet_01v8 L=0.5 W=12 nf=1 ad='int((nf+1)/2) * W/nf * 0.29' as='int((nf+2)/2) * W/nf * 0.29'
+ pd='2*int((nf+1)/2) * (W/nf + 0.29)' ps='2*int((nf+2)/2) * (W/nf + 0.29)' nrd='0.29 / W' nrs='0.29 / W'
+ sa=0 sb=0 sd=0 mult=1 m=1
XM109 GND GND GND GND sky130_fd_pr__nfet_01v8 L=0.5 W=12 nf=1 ad='int((nf+1)/2) * W/nf * 0.29' as='int((nf+2)/2) * W/nf * 0.29'
+ pd='2*int((nf+1)/2) * (W/nf + 0.29)' ps='2*int((nf+2)/2) * (W/nf + 0.29)' nrd='0.29 / W' nrs='0.29 / W'
+ sa=0 sb=0 sd=0 mult=1 m=1
XM20 GND Vout net5 GND sky130_fd_pr__nfet_01v8 L=0.5 W=12 nf=1 ad='int((nf+1)/2) * W/nf * 0.29' as='int((nf+2)/2) * W/nf * 0.29'
+ pd='2*int((nf+1)/2) * (W/nf + 0.29)' ps='2*int((nf+2)/2) * (W/nf + 0.29)' nrd='0.29 / W' nrs='0.29 / W'
+ sa=0 sb=0 sd=0 mult=1 m=1
XM19 net6 Vout GND GND sky130_fd_pr__nfet_01v8 L=0.5 W=12 nf=1 ad='int((nf+1)/2) * W/nf * 0.29' as='int((nf+2)/2) * W/nf * 0.29'
+ pd='2*int((nf+1)/2) * (W/nf + 0.29)' ps='2*int((nf+2)/2) * (W/nf + 0.29)' nrd='0.29 / W' nrs='0.29 / W'
+ sa=0 sb=0 sd=0 mult=1 m=1
XM18 GND Vout net5 GND sky130_fd_pr__nfet_01v8 L=0.5 W=12 nf=1 ad='int((nf+1)/2) * W/nf * 0.29' as='int((nf+2)/2) * W/nf * 0.29'
+ pd='2*int((nf+1)/2) * (W/nf + 0.29)' ps='2*int((nf+2)/2) * (W/nf + 0.29)' nrd='0.29 / W' nrs='0.29 / W'
+ sa=0 sb=0 sd=0 mult=1 m=1
XM17 net6 Vout GND GND sky130_fd_pr__nfet_01v8 L=0.5 W=12 nf=1 ad='int((nf+1)/2) * W/nf * 0.29' as='int((nf+2)/2) * W/nf * 0.29'
+ pd='2*int((nf+1)/2) * (W/nf + 0.29)' ps='2*int((nf+2)/2) * (W/nf + 0.29)' nrd='0.29 / W' nrs='0.29 / W'
+ sa=0 sb=0 sd=0 mult=1 m=1
XM85 GND Vout net6 GND sky130_fd_pr__nfet_01v8 L=0.5 W=12 nf=1 ad='int((nf+1)/2) * W/nf * 0.29' as='int((nf+2)/2) * W/nf * 0.29'
+ pd='2*int((nf+1)/2) * (W/nf + 0.29)' ps='2*int((nf+2)/2) * (W/nf + 0.29)' nrd='0.29 / W' nrs='0.29 / W'
+ sa=0 sb=0 sd=0 mult=1 m=1
XM86 net5 Vout GND GND sky130_fd_pr__nfet_01v8 L=0.5 W=12 nf=1 ad='int((nf+1)/2) * W/nf * 0.29' as='int((nf+2)/2) * W/nf * 0.29'
+ pd='2*int((nf+1)/2) * (W/nf + 0.29)' ps='2*int((nf+2)/2) * (W/nf + 0.29)' nrd='0.29 / W' nrs='0.29 / W'
+ sa=0 sb=0 sd=0 mult=1 m=1
XM87 GND Vout net6 GND sky130_fd_pr__nfet_01v8 L=0.5 W=12 nf=1 ad='int((nf+1)/2) * W/nf * 0.29' as='int((nf+2)/2) * W/nf * 0.29'
+ pd='2*int((nf+1)/2) * (W/nf + 0.29)' ps='2*int((nf+2)/2) * (W/nf + 0.29)' nrd='0.29 / W' nrs='0.29 / W'
+ sa=0 sb=0 sd=0 mult=1 m=1
XM88 net5 Vout GND GND sky130_fd_pr__nfet_01v8 L=0.5 W=12 nf=1 ad='int((nf+1)/2) * W/nf * 0.29' as='int((nf+2)/2) * W/nf * 0.29'
+ pd='2*int((nf+1)/2) * (W/nf + 0.29)' ps='2*int((nf+2)/2) * (W/nf + 0.29)' nrd='0.29 / W' nrs='0.29 / W'
+ sa=0 sb=0 sd=0 mult=1 m=1
XM110 GND GND GND GND sky130_fd_pr__nfet_01v8 L=0.5 W=12 nf=1 ad='int((nf+1)/2) * W/nf * 0.29' as='int((nf+2)/2) * W/nf * 0.29'
+ pd='2*int((nf+1)/2) * (W/nf + 0.29)' ps='2*int((nf+2)/2) * (W/nf + 0.29)' nrd='0.29 / W' nrs='0.29 / W'
+ sa=0 sb=0 sd=0 mult=1 m=1
**.ends
.end
